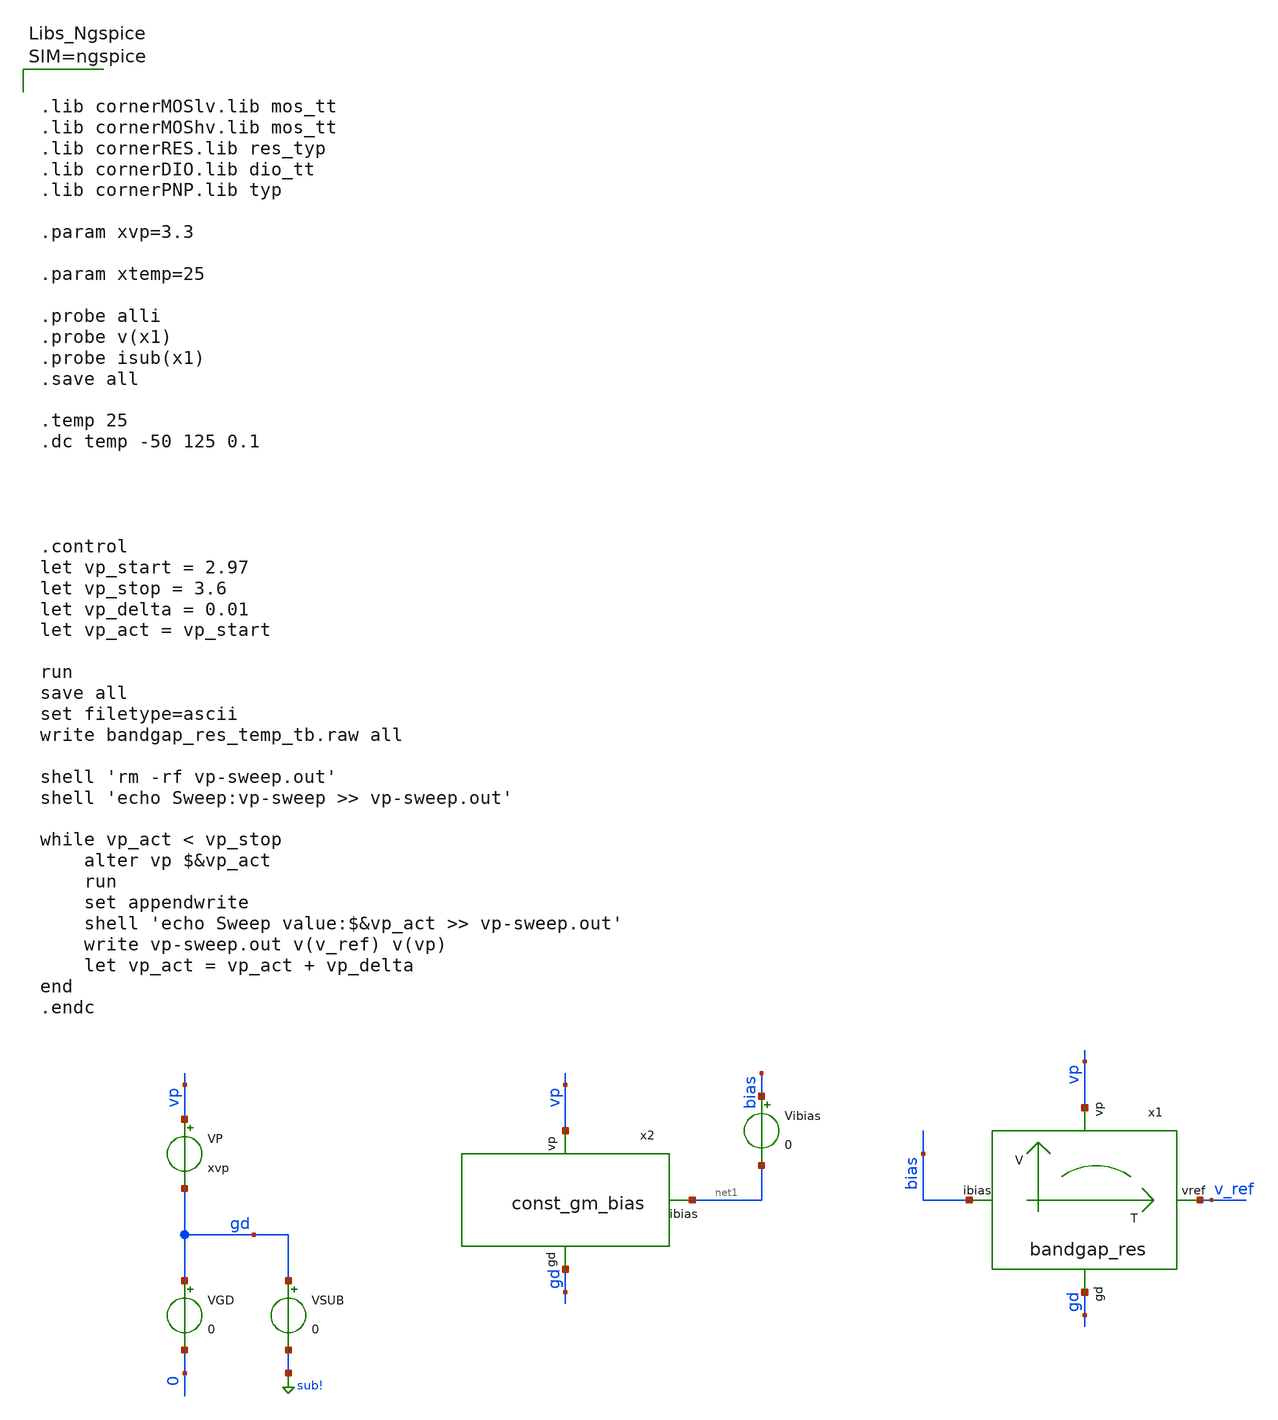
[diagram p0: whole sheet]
** sch_path: bandgap_res_tb/bandgap_res_temp_tb.sch
**.subckt bandgap_res_temp_tb
x1 vp bias v_ref gd bandgap_res
VGD gd 0 0
VP vp gd xvp
.save i(vp)
VSUB gd sub! 0
x2 vp net1 gd const_gm_bias
Vibias bias net1 0
.save i(vibias)
**** begin user architecture code



.lib cornerMOSlv.lib mos_tt
.lib cornerMOShv.lib mos_tt
.lib cornerRES.lib res_typ
.lib cornerDIO.lib dio_tt
.lib cornerPNP.lib typ

.param xvp=3.3

.param xtemp=25

.probe alli
.probe v(x1)
.probe isub(x1)
.save all

.temp 25
.dc temp -50 125 0.1




.control
let vp_start = 2.97
let vp_stop = 3.6
let vp_delta = 0.01
let vp_act = vp_start

run
save all
set filetype=ascii
write bandgap_res_temp_tb.raw all

shell 'rm -rf vp-sweep.out'
shell 'echo Sweep:vp-sweep >> vp-sweep.out'

while vp_act < vp_stop
	alter vp $&vp_act
	run
	set appendwrite
	shell 'echo Sweep value:$&vp_act >> vp-sweep.out'
	write vp-sweep.out v(v_ref) v(vp)
	let vp_act = vp_act + vp_delta
end
.endc



**** end user architecture code
**.ends
.GLOBAL sub!
.end
